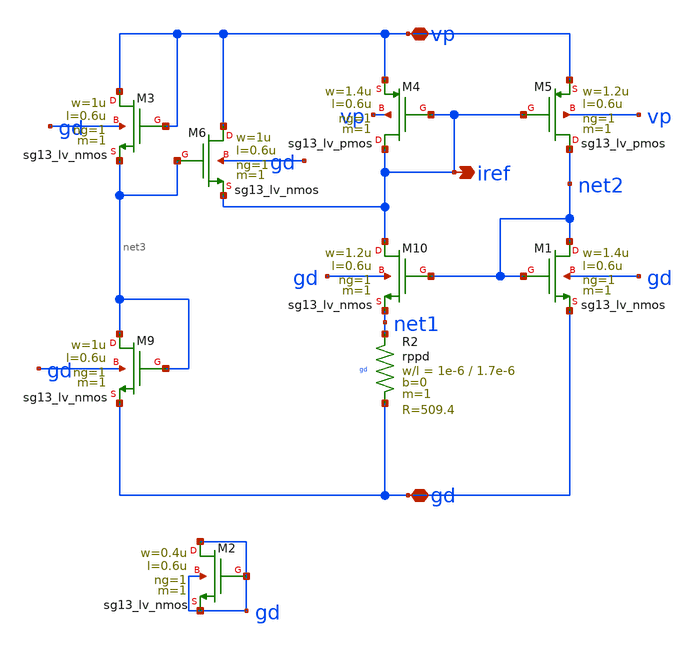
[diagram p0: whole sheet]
** sch_path: PLL0663-main/schematic/xschem/charge_pump/curr_source.sch
**.subckt curr_source vp gd iref
*.iopin vp
*.iopin gd
*.opin iref
XM9 net3 net3 gd gd sg13_lv_nmos w=1u l=0.6u ng=1 m=1 mm_ok=1
XM4 iref iref vp vp sg13_lv_pmos w=1.4u l=0.6u ng=1 m=1 mm_ok=1
XM5 net2 iref vp vp sg13_lv_pmos w=1.2u l=0.6u ng=1 m=1 mm_ok=1
XM10 iref net2 net1 gd sg13_lv_nmos w=1.2u l=0.6u ng=1 m=1 mm_ok=1
XM1 net2 net2 gd gd sg13_lv_nmos w=1.4u l=0.6u ng=1 m=1 mm_ok=1
XM3 vp vp net3 gd sg13_lv_nmos w=1u l=0.6u ng=1 m=1 mm_ok=1
XM6 vp net3 iref gd sg13_lv_nmos w=1u l=0.6u ng=1 m=1 mm_ok=1
XM2 gd gd gd gd sg13_lv_nmos w=0.4u l=0.6u ng=1 m=1 mm_ok=1
XR2 net1 gd gd rppd w=1e-6 l=1.7e-6 m=1 b=0 mm_ok=1
**.ends
.end
